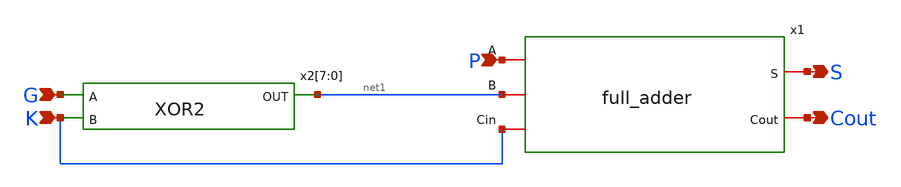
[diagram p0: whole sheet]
** sch_path: design/xschem/SUBTRACTOR/subtractor.sch
**.subckt subtractor P G S Cout K
*.ipin P
*.ipin G
*.opin S
*.opin Cout
*.ipin K
x1 P S net1 K Cout full_adder
x2[7] G K net1 XOR2
x2[6] G K net1 XOR2
x2[5] G K net1 XOR2
x2[4] G K net1 XOR2
x2[3] G K net1 XOR2
x2[2] G K net1 XOR2
x2[1] G K net1 XOR2
x2[0] G K net1 XOR2
**.ends
.end
